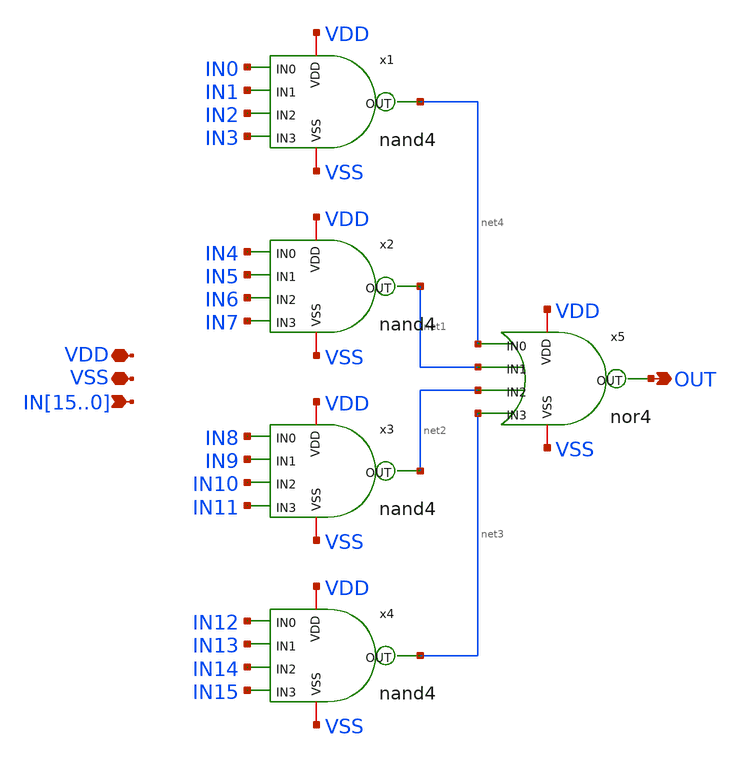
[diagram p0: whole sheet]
** sch_path: CAD4/and16.sch
**.subckt and16 VSS VDD IN15,IN14,IN13,IN12,IN11,IN10,IN9,IN8,IN7,IN6,IN5,IN4,IN3,IN2,IN1,IN0 OUT
*.iopin VSS
*.iopin VDD
*.ipin IN15,IN14,IN13,IN12,IN11,IN10,IN9,IN8,IN7,IN6,IN5,IN4,IN3,IN2,IN1,IN0
*.opin OUT
x1 net4 VSS VDD IN0 IN1 IN2 IN3 nand4
x2 net1 VSS VDD IN4 IN5 IN6 IN7 nand4
x3 net2 VSS VDD IN8 IN9 IN10 IN11 nand4
x4 net3 VSS VDD IN12 IN13 IN14 IN15 nand4
x5 OUT VSS VDD net4 net1 net2 net3 nor4
**.ends

* expanding   symbol:  engn1600-team1/CAD4/nand4.sym # of pins=7
** sym_path: CAD4/nand4.sym
** sch_path: CAD4/nand4.sch
.subckt nand4 OUT VSS VDD IN0 IN1 IN2 IN3
*.iopin VSS
*.iopin VDD
*.ipin IN0
*.ipin IN1
*.opin OUT
*.ipin IN2
*.ipin IN3
XM1 net1 IN2 net2 VSS nfet_03v3 L=0.28u W=0.36u nf=1 ad='int((nf+1)/2) * W/nf * 0.18u' as='int((nf+2)/2) * W/nf * 0.18u'
+ pd='2*int((nf+1)/2) * (W/nf + 0.18u)' ps='2*int((nf+2)/2) * (W/nf + 0.18u)' nrd='0.18u / W' nrs='0.18u / W'
+ sa=0 sb=0 sd=0 m=1
XM2 OUT IN3 net1 VSS nfet_03v3 L=0.28u W=0.36u nf=1 ad='int((nf+1)/2) * W/nf * 0.18u' as='int((nf+2)/2) * W/nf * 0.18u'
+ pd='2*int((nf+1)/2) * (W/nf + 0.18u)' ps='2*int((nf+2)/2) * (W/nf + 0.18u)' nrd='0.18u / W' nrs='0.18u / W'
+ sa=0 sb=0 sd=0 m=1
XM3 OUT IN1 VDD VDD pfet_03v3 L=0.28u W=0.36u nf=1 ad='int((nf+1)/2) * W/nf * 0.18u' as='int((nf+2)/2) * W/nf * 0.18u'
+ pd='2*int((nf+1)/2) * (W/nf + 0.18u)' ps='2*int((nf+2)/2) * (W/nf + 0.18u)' nrd='0.18u / W' nrs='0.18u / W'
+ sa=0 sb=0 sd=0 m=1
XM4 OUT IN2 VDD VDD pfet_03v3 L=0.28u W=0.36u nf=1 ad='int((nf+1)/2) * W/nf * 0.18u' as='int((nf+2)/2) * W/nf * 0.18u'
+ pd='2*int((nf+1)/2) * (W/nf + 0.18u)' ps='2*int((nf+2)/2) * (W/nf + 0.18u)' nrd='0.18u / W' nrs='0.18u / W'
+ sa=0 sb=0 sd=0 m=1
XM5 OUT IN0 VDD VDD pfet_03v3 L=0.28u W=0.36u nf=1 ad='int((nf+1)/2) * W/nf * 0.18u' as='int((nf+2)/2) * W/nf * 0.18u'
+ pd='2*int((nf+1)/2) * (W/nf + 0.18u)' ps='2*int((nf+2)/2) * (W/nf + 0.18u)' nrd='0.18u / W' nrs='0.18u / W'
+ sa=0 sb=0 sd=0 m=1
XM6 OUT IN3 VDD VDD pfet_03v3 L=0.28u W=0.36u nf=1 ad='int((nf+1)/2) * W/nf * 0.18u' as='int((nf+2)/2) * W/nf * 0.18u'
+ pd='2*int((nf+1)/2) * (W/nf + 0.18u)' ps='2*int((nf+2)/2) * (W/nf + 0.18u)' nrd='0.18u / W' nrs='0.18u / W'
+ sa=0 sb=0 sd=0 m=1
XM7 net3 IN0 VSS VSS nfet_03v3 L=0.28u W=0.36u nf=1 ad='int((nf+1)/2) * W/nf * 0.18u' as='int((nf+2)/2) * W/nf * 0.18u'
+ pd='2*int((nf+1)/2) * (W/nf + 0.18u)' ps='2*int((nf+2)/2) * (W/nf + 0.18u)' nrd='0.18u / W' nrs='0.18u / W'
+ sa=0 sb=0 sd=0 m=1
XM8 net2 IN1 net3 VSS nfet_03v3 L=0.28u W=0.36u nf=1 ad='int((nf+1)/2) * W/nf * 0.18u' as='int((nf+2)/2) * W/nf * 0.18u'
+ pd='2*int((nf+1)/2) * (W/nf + 0.18u)' ps='2*int((nf+2)/2) * (W/nf + 0.18u)' nrd='0.18u / W' nrs='0.18u / W'
+ sa=0 sb=0 sd=0 m=1
.ends


* expanding   symbol:  engn1600-team1/CAD4/nor4.sym # of pins=7
** sym_path: CAD4/nor4.sym
** sch_path: CAD4/nor4.sch
.subckt nor4 OUT VSS VDD IN0 IN1 IN2 IN3
*.iopin VSS
*.iopin VDD
*.ipin IN0
*.ipin IN1
*.opin OUT
*.ipin IN2
*.ipin IN3
XM1 net1 IN1 net2 VDD pfet_03v3 L=0.28u W=0.36u nf=1 ad='int((nf+1)/2) * W/nf * 0.18u' as='int((nf+2)/2) * W/nf * 0.18u'
+ pd='2*int((nf+1)/2) * (W/nf + 0.18u)' ps='2*int((nf+2)/2) * (W/nf + 0.18u)' nrd='0.18u / W' nrs='0.18u / W'
+ sa=0 sb=0 sd=0 m=1
XM2 net2 IN0 VDD VDD pfet_03v3 L=0.28u W=0.36u nf=1 ad='int((nf+1)/2) * W/nf * 0.18u' as='int((nf+2)/2) * W/nf * 0.18u'
+ pd='2*int((nf+1)/2) * (W/nf + 0.18u)' ps='2*int((nf+2)/2) * (W/nf + 0.18u)' nrd='0.18u / W' nrs='0.18u / W'
+ sa=0 sb=0 sd=0 m=1
XM3 OUT IN1 VSS OUT nfet_03v3 L=0.28u W=0.36u nf=1 ad='int((nf+1)/2) * W/nf * 0.18u' as='int((nf+2)/2) * W/nf * 0.18u'
+ pd='2*int((nf+1)/2) * (W/nf + 0.18u)' ps='2*int((nf+2)/2) * (W/nf + 0.18u)' nrd='0.18u / W' nrs='0.18u / W'
+ sa=0 sb=0 sd=0 m=1
XM4 OUT IN2 VSS OUT nfet_03v3 L=0.28u W=0.36u nf=1 ad='int((nf+1)/2) * W/nf * 0.18u' as='int((nf+2)/2) * W/nf * 0.18u'
+ pd='2*int((nf+1)/2) * (W/nf + 0.18u)' ps='2*int((nf+2)/2) * (W/nf + 0.18u)' nrd='0.18u / W' nrs='0.18u / W'
+ sa=0 sb=0 sd=0 m=1
XM5 OUT IN0 VSS OUT nfet_03v3 L=0.28u W=0.36u nf=1 ad='int((nf+1)/2) * W/nf * 0.18u' as='int((nf+2)/2) * W/nf * 0.18u'
+ pd='2*int((nf+1)/2) * (W/nf + 0.18u)' ps='2*int((nf+2)/2) * (W/nf + 0.18u)' nrd='0.18u / W' nrs='0.18u / W'
+ sa=0 sb=0 sd=0 m=1
XM6 OUT IN3 VSS OUT nfet_03v3 L=0.28u W=0.36u nf=1 ad='int((nf+1)/2) * W/nf * 0.18u' as='int((nf+2)/2) * W/nf * 0.18u'
+ pd='2*int((nf+1)/2) * (W/nf + 0.18u)' ps='2*int((nf+2)/2) * (W/nf + 0.18u)' nrd='0.18u / W' nrs='0.18u / W'
+ sa=0 sb=0 sd=0 m=1
XM7 OUT IN3 net3 VDD pfet_03v3 L=0.28u W=0.36u nf=1 ad='int((nf+1)/2) * W/nf * 0.18u' as='int((nf+2)/2) * W/nf * 0.18u'
+ pd='2*int((nf+1)/2) * (W/nf + 0.18u)' ps='2*int((nf+2)/2) * (W/nf + 0.18u)' nrd='0.18u / W' nrs='0.18u / W'
+ sa=0 sb=0 sd=0 m=1
XM8 net3 IN2 net1 VDD pfet_03v3 L=0.28u W=0.36u nf=1 ad='int((nf+1)/2) * W/nf * 0.18u' as='int((nf+2)/2) * W/nf * 0.18u'
+ pd='2*int((nf+1)/2) * (W/nf + 0.18u)' ps='2*int((nf+2)/2) * (W/nf + 0.18u)' nrd='0.18u / W' nrs='0.18u / W'
+ sa=0 sb=0 sd=0 m=1
.ends

.end
